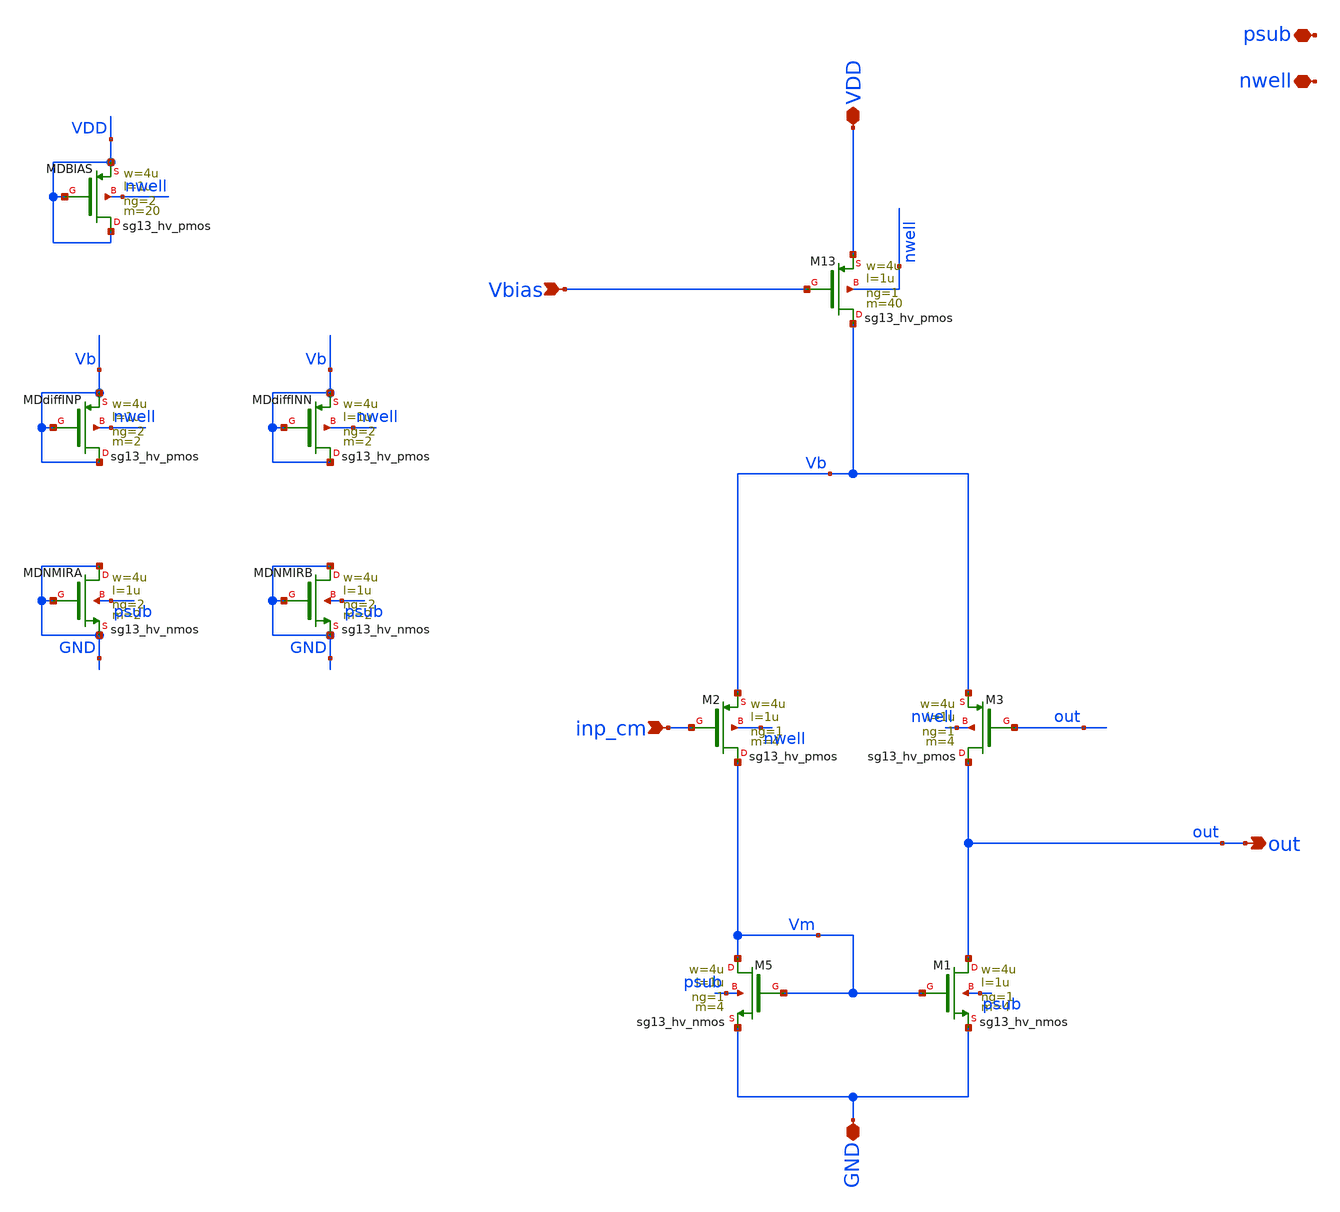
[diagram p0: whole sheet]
** sch_path: xschem/analog_buffer.sch
**.subckt analog_buffer inp_cm out VDD GND Vbias psub nwell
*.ipin inp_cm
*.opin out
*.iopin VDD
*.iopin GND
*.ipin Vbias
*.iopin psub
*.iopin nwell
XM2 Vm inp_cm Vb nwell sg13_hv_pmos w=4u l=1u ng=1 m=4 mm_ok=1
XM5 Vm Vm GND psub sg13_hv_nmos w=4u l=1u ng=1 m=4 mm_ok=1
XM13 Vb Vbias VDD nwell sg13_hv_pmos w=4u l=1u ng=1 m=40 mm_ok=1
XM3 out out Vb nwell sg13_hv_pmos w=4u l=1u ng=1 m=4 mm_ok=1
XM1 out Vm GND psub sg13_hv_nmos w=4u l=1u ng=1 m=4 mm_ok=1
XMDBIAS VDD VDD VDD nwell sg13_hv_pmos w=4u l=1u ng=2 m=20 mm_ok=1
XMDdiffINP Vb Vb Vb nwell sg13_hv_pmos w=4u l=1u ng=2 m=2 mm_ok=1
XMDdiffINN Vb Vb Vb nwell sg13_hv_pmos w=4u l=1u ng=2 m=2 mm_ok=1
XMDNMIRA GND GND GND psub sg13_hv_nmos w=4u l=1u ng=2 m=2 mm_ok=1
XMDNMIRB GND GND GND psub sg13_hv_nmos w=4u l=1u ng=2 m=2 mm_ok=1
**.ends
.end
